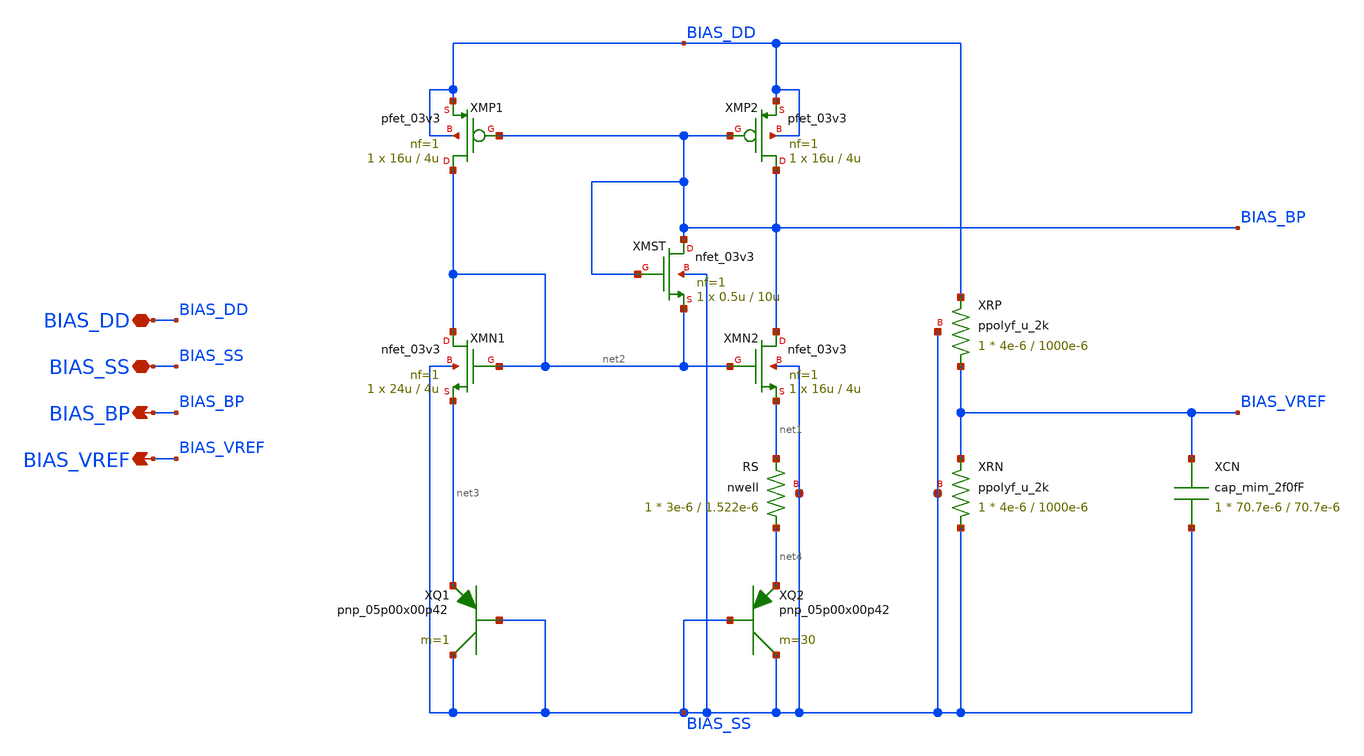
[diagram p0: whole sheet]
** sch_path: Design_Files/IC Design/Schematic/BIAS/BIAS.sch
**.subckt BIAS BIAS_DD BIAS_SS BIAS_BP BIAS_VREF
*.iopin BIAS_DD
*.iopin BIAS_SS
*.opin BIAS_BP
*.opin BIAS_VREF
XMN2 BIAS_BP net2 net1 BIAS_SS nfet_03v3 L=4u W=16u nf=1 ad='int((nf+1)/2) * W/nf * 0.18u' as='int((nf+2)/2) * W/nf * 0.18u'
+ pd='2*int((nf+1)/2) * (W/nf + 0.18u)' ps='2*int((nf+2)/2) * (W/nf + 0.18u)' nrd='0.18u / W' nrs='0.18u / W'
+ sa=0 sb=0 sd=0 m=1
XMP2 BIAS_BP BIAS_BP BIAS_DD BIAS_DD pfet_03v3 L=4u W=16u nf=1 ad='int((nf+1)/2) * W/nf * 0.18u' as='int((nf+2)/2) * W/nf * 0.18u'
+ pd='2*int((nf+1)/2) * (W/nf + 0.18u)' ps='2*int((nf+2)/2) * (W/nf + 0.18u)' nrd='0.18u / W' nrs='0.18u / W'
+ sa=0 sb=0 sd=0 m=1
XMN1 net2 net2 net3 BIAS_SS nfet_03v3 L=4u W=24u nf=1 ad='int((nf+1)/2) * W/nf * 0.18u' as='int((nf+2)/2) * W/nf * 0.18u'
+ pd='2*int((nf+1)/2) * (W/nf + 0.18u)' ps='2*int((nf+2)/2) * (W/nf + 0.18u)' nrd='0.18u / W' nrs='0.18u / W'
+ sa=0 sb=0 sd=0 m=1
XMP1 net2 BIAS_BP BIAS_DD BIAS_DD pfet_03v3 L=4u W=16u nf=1 ad='int((nf+1)/2) * W/nf * 0.18u' as='int((nf+2)/2) * W/nf * 0.18u'
+ pd='2*int((nf+1)/2) * (W/nf + 0.18u)' ps='2*int((nf+2)/2) * (W/nf + 0.18u)' nrd='0.18u / W' nrs='0.18u / W'
+ sa=0 sb=0 sd=0 m=1
XMST BIAS_BP BIAS_BP net2 BIAS_SS nfet_03v3 L=10u W=0.5u nf=1 ad='int((nf+1)/2) * W/nf * 0.18u' as='int((nf+2)/2) * W/nf * 0.18u'
+ pd='2*int((nf+1)/2) * (W/nf + 0.18u)' ps='2*int((nf+2)/2) * (W/nf + 0.18u)' nrd='0.18u / W' nrs='0.18u / W'
+ sa=0 sb=0 sd=0 m=1
XRP BIAS_VREF BIAS_DD BIAS_SS ppolyf_u_2k r_width=4e-6 r_length=1000e-6 m=1
XRN BIAS_SS BIAS_VREF BIAS_SS ppolyf_u_2k r_width=4e-6 r_length=1000e-6 m=1
XCN BIAS_VREF BIAS_SS cap_mim_2f0fF c_width=70.7e-6 c_length=70.7e-6 m=1
XQ1 BIAS_SS BIAS_SS net3 pnp_05p00x00p42 m=1 par=1
XQ2 BIAS_SS BIAS_SS net4 pnp_05p00x00p42 m=30 par=30
XRS net4 net1 BIAS_SS nwell r_width=3e-6 r_length=1.522e-6 m=1
**.ends
.end
